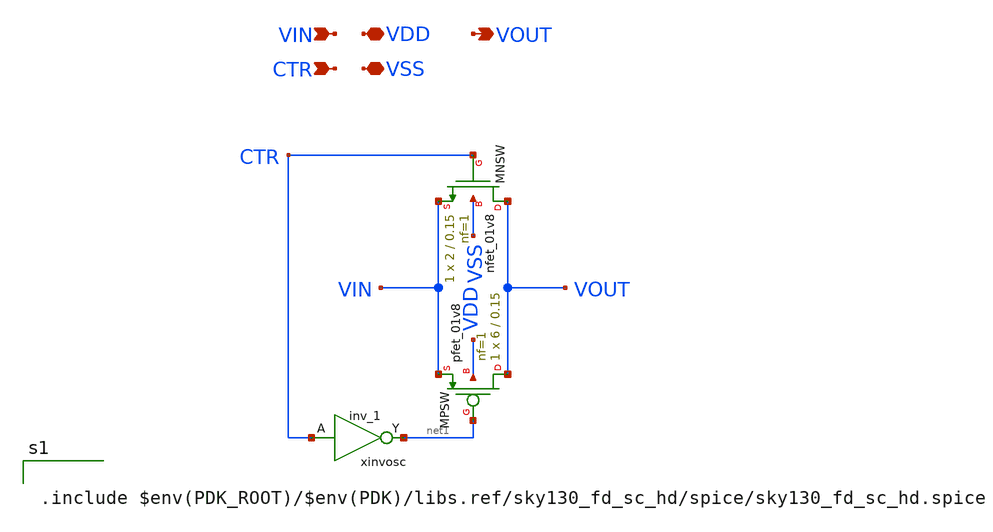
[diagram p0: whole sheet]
** sch_path: modules/PASSGATE/symbol/PASSGATE.sch
**.subckt PASSGATE VIN VDD VSS CTR VOUT
*.ipin VIN
*.iopin VDD
*.iopin VSS
*.ipin CTR
*.opin VOUT
XMNSW VOUT CTR VIN VSS sky130_fd_pr__nfet_01v8 L=0.15 W=2 nf=1 ad='int((nf+1)/2) * W/nf * 0.29' as='int((nf+2)/2) * W/nf * 0.29'
+ pd='2*int((nf+1)/2) * (W/nf + 0.29)' ps='2*int((nf+2)/2) * (W/nf + 0.29)' nrd='0.29 / W' nrs='0.29 / W'
+ sa=0 sb=0 sd=0 mult=1 m=1
XMPSW VOUT net1 VIN VDD sky130_fd_pr__pfet_01v8 L=0.15 W=6 nf=1 ad='int((nf+1)/2) * W/nf * 0.29' as='int((nf+2)/2) * W/nf * 0.29'
+ pd='2*int((nf+1)/2) * (W/nf + 0.29)' ps='2*int((nf+2)/2) * (W/nf + 0.29)' nrd='0.29 / W' nrs='0.29 / W'
+ sa=0 sb=0 sd=0 mult=1 m=1
xinvosc CTR VSS VSS VDD VDD net1 sky130_fd_sc_hd__inv_1
**** begin user architecture code

.include $env(PDK_ROOT)/$env(PDK)/libs.ref/sky130_fd_sc_hd/spice/sky130_fd_sc_hd.spice

**** end user architecture code
**.ends
.end
